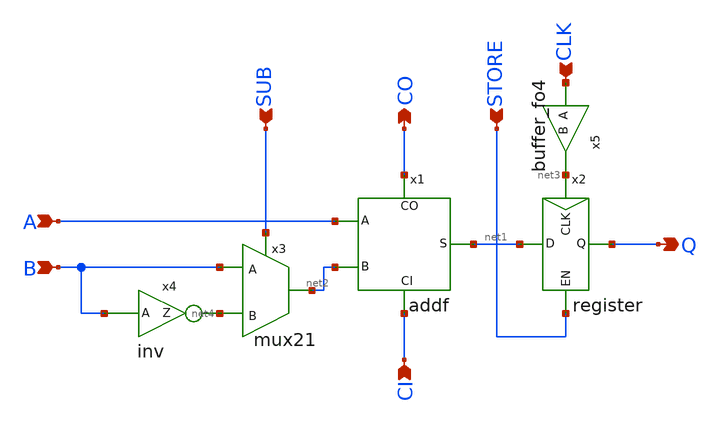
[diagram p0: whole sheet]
** sch_path: xschem/bitslice.sch
**.subckt bitslice A B CI CLK STORE CO Q SUB
*.ipin A
*.ipin B
*.ipin CI
*.ipin CLK
*.ipin STORE
*.opin CO
*.opin Q
*.ipin SUB
x1 A net2 CI net1 CO addf
x2 net3 STORE Q net1 register
x3 SUB B net2 net4 mux21
x4 net4 B inv
x5 net3 CLK buffer_fo4
**.ends

* expanding   symbol:  addf.sym # of pins=5
** sym_path: xschem/addf.sym
** sch_path: xschem/addf.sch
.subckt addf A B CI S CO
*.ipin A
*.ipin B
*.ipin CI
*.opin S
*.opin CO
XM1 theta CI mu GND sky130_fd_pr__nfet_01v8 L=0.15 W=0.42 nf=1 ad='int((nf+1)/2) * W/nf * 0.29' as='int((nf+2)/2) * W/nf * 0.29'
+ pd='2*int((nf+1)/2) * (W/nf + 0.29)' ps='2*int((nf+2)/2) * (W/nf + 0.29)' nrd='0.29 / W' nrs='0.29 / W'
+ sa=0 sb=0 sd=0 mult=1 m=1
XM2 theta CI lambda VDD sky130_fd_pr__pfet_01v8 L=0.15 W=0.42 nf=1 ad='int((nf+1)/2) * W/nf * 0.29' as='int((nf+2)/2) * W/nf * 0.29'
+ pd='2*int((nf+1)/2) * (W/nf + 0.29)' ps='2*int((nf+2)/2) * (W/nf + 0.29)' nrd='0.29 / W' nrs='0.29 / W'
+ sa=0 sb=0 sd=0 mult=1 m=1
XM3 lambda A VDD VDD sky130_fd_pr__pfet_01v8 L=0.15 W=0.42 nf=1 ad='int((nf+1)/2) * W/nf * 0.29' as='int((nf+2)/2) * W/nf * 0.29'
+ pd='2*int((nf+1)/2) * (W/nf + 0.29)' ps='2*int((nf+2)/2) * (W/nf + 0.29)' nrd='0.29 / W' nrs='0.29 / W'
+ sa=0 sb=0 sd=0 mult=1 m=1
XM4 lambda B VDD VDD sky130_fd_pr__pfet_01v8 L=0.15 W=0.42 nf=1 ad='int((nf+1)/2) * W/nf * 0.29' as='int((nf+2)/2) * W/nf * 0.29'
+ pd='2*int((nf+1)/2) * (W/nf + 0.29)' ps='2*int((nf+2)/2) * (W/nf + 0.29)' nrd='0.29 / W' nrs='0.29 / W'
+ sa=0 sb=0 sd=0 mult=1 m=1
XM5 mu A GND GND sky130_fd_pr__nfet_01v8 L=0.15 W=0.42 nf=1 ad='int((nf+1)/2) * W/nf * 0.29' as='int((nf+2)/2) * W/nf * 0.29'
+ pd='2*int((nf+1)/2) * (W/nf + 0.29)' ps='2*int((nf+2)/2) * (W/nf + 0.29)' nrd='0.29 / W' nrs='0.29 / W'
+ sa=0 sb=0 sd=0 mult=1 m=1
XM6 mu B GND GND sky130_fd_pr__nfet_01v8 L=0.15 W=0.42 nf=1 ad='int((nf+1)/2) * W/nf * 0.29' as='int((nf+2)/2) * W/nf * 0.29'
+ pd='2*int((nf+1)/2) * (W/nf + 0.29)' ps='2*int((nf+2)/2) * (W/nf + 0.29)' nrd='0.29 / W' nrs='0.29 / W'
+ sa=0 sb=0 sd=0 mult=1 m=1
XM7 theta B iota VDD sky130_fd_pr__pfet_01v8 L=0.15 W=0.42 nf=1 ad='int((nf+1)/2) * W/nf * 0.29' as='int((nf+2)/2) * W/nf * 0.29'
+ pd='2*int((nf+1)/2) * (W/nf + 0.29)' ps='2*int((nf+2)/2) * (W/nf + 0.29)' nrd='0.29 / W' nrs='0.29 / W'
+ sa=0 sb=0 sd=0 mult=1 m=1
XM8 iota A VDD VDD sky130_fd_pr__pfet_01v8 L=0.15 W=0.42 nf=1 ad='int((nf+1)/2) * W/nf * 0.29' as='int((nf+2)/2) * W/nf * 0.29'
+ pd='2*int((nf+1)/2) * (W/nf + 0.29)' ps='2*int((nf+2)/2) * (W/nf + 0.29)' nrd='0.29 / W' nrs='0.29 / W'
+ sa=0 sb=0 sd=0 mult=1 m=1
XM9 theta B kappa GND sky130_fd_pr__nfet_01v8 L=0.15 W=0.42 nf=1 ad='int((nf+1)/2) * W/nf * 0.29' as='int((nf+2)/2) * W/nf * 0.29'
+ pd='2*int((nf+1)/2) * (W/nf + 0.29)' ps='2*int((nf+2)/2) * (W/nf + 0.29)' nrd='0.29 / W' nrs='0.29 / W'
+ sa=0 sb=0 sd=0 mult=1 m=1
XM10 kappa A GND GND sky130_fd_pr__nfet_01v8 L=0.15 W=0.42 nf=1 ad='int((nf+1)/2) * W/nf * 0.29' as='int((nf+2)/2) * W/nf * 0.29'
+ pd='2*int((nf+1)/2) * (W/nf + 0.29)' ps='2*int((nf+2)/2) * (W/nf + 0.29)' nrd='0.29 / W' nrs='0.29 / W'
+ sa=0 sb=0 sd=0 mult=1 m=1
XM11 epsilon A VDD VDD sky130_fd_pr__pfet_01v8 L=0.15 W=0.42 nf=1 ad='int((nf+1)/2) * W/nf * 0.29' as='int((nf+2)/2) * W/nf * 0.29'
+ pd='2*int((nf+1)/2) * (W/nf + 0.29)' ps='2*int((nf+2)/2) * (W/nf + 0.29)' nrd='0.29 / W' nrs='0.29 / W'
+ sa=0 sb=0 sd=0 mult=1 m=1
XM12 epsilon B VDD VDD sky130_fd_pr__pfet_01v8 L=0.15 W=0.42 nf=1 ad='int((nf+1)/2) * W/nf * 0.29' as='int((nf+2)/2) * W/nf * 0.29'
+ pd='2*int((nf+1)/2) * (W/nf + 0.29)' ps='2*int((nf+2)/2) * (W/nf + 0.29)' nrd='0.29 / W' nrs='0.29 / W'
+ sa=0 sb=0 sd=0 mult=1 m=1
XM13 epsilon CI VDD VDD sky130_fd_pr__pfet_01v8 L=0.15 W=0.42 nf=1 ad='int((nf+1)/2) * W/nf * 0.29' as='int((nf+2)/2) * W/nf * 0.29'
+ pd='2*int((nf+1)/2) * (W/nf + 0.29)' ps='2*int((nf+2)/2) * (W/nf + 0.29)' nrd='0.29 / W' nrs='0.29 / W'
+ sa=0 sb=0 sd=0 mult=1 m=1
XM14 COM theta epsilon VDD sky130_fd_pr__pfet_01v8 L=0.15 W=0.42 nf=1 ad='int((nf+1)/2) * W/nf * 0.29'
+ as='int((nf+2)/2) * W/nf * 0.29' pd='2*int((nf+1)/2) * (W/nf + 0.29)' ps='2*int((nf+2)/2) * (W/nf + 0.29)'
+ nrd='0.29 / W' nrs='0.29 / W' sa=0 sb=0 sd=0 mult=1 m=1
XM15 COM theta zeta GND sky130_fd_pr__nfet_01v8 L=0.15 W=0.42 nf=1 ad='int((nf+1)/2) * W/nf * 0.29' as='int((nf+2)/2) * W/nf * 0.29'
+ pd='2*int((nf+1)/2) * (W/nf + 0.29)' ps='2*int((nf+2)/2) * (W/nf + 0.29)' nrd='0.29 / W' nrs='0.29 / W'
+ sa=0 sb=0 sd=0 mult=1 m=1
XM16 zeta A GND GND sky130_fd_pr__nfet_01v8 L=0.15 W=0.42 nf=1 ad='int((nf+1)/2) * W/nf * 0.29' as='int((nf+2)/2) * W/nf * 0.29'
+ pd='2*int((nf+1)/2) * (W/nf + 0.29)' ps='2*int((nf+2)/2) * (W/nf + 0.29)' nrd='0.29 / W' nrs='0.29 / W'
+ sa=0 sb=0 sd=0 mult=1 m=1
XM17 zeta B GND GND sky130_fd_pr__nfet_01v8 L=0.15 W=0.42 nf=1 ad='int((nf+1)/2) * W/nf * 0.29' as='int((nf+2)/2) * W/nf * 0.29'
+ pd='2*int((nf+1)/2) * (W/nf + 0.29)' ps='2*int((nf+2)/2) * (W/nf + 0.29)' nrd='0.29 / W' nrs='0.29 / W'
+ sa=0 sb=0 sd=0 mult=1 m=1
XM18 zeta CI GND GND sky130_fd_pr__nfet_01v8 L=0.15 W=0.42 nf=1 ad='int((nf+1)/2) * W/nf * 0.29' as='int((nf+2)/2) * W/nf * 0.29'
+ pd='2*int((nf+1)/2) * (W/nf + 0.29)' ps='2*int((nf+2)/2) * (W/nf + 0.29)' nrd='0.29 / W' nrs='0.29 / W'
+ sa=0 sb=0 sd=0 mult=1 m=1
XM19 COM B beta VDD sky130_fd_pr__pfet_01v8 L=0.15 W=0.42 nf=1 ad='int((nf+1)/2) * W/nf * 0.29' as='int((nf+2)/2) * W/nf * 0.29'
+ pd='2*int((nf+1)/2) * (W/nf + 0.29)' ps='2*int((nf+2)/2) * (W/nf + 0.29)' nrd='0.29 / W' nrs='0.29 / W'
+ sa=0 sb=0 sd=0 mult=1 m=1
XM20 beta CI alpha VDD sky130_fd_pr__pfet_01v8 L=0.15 W=0.42 nf=1 ad='int((nf+1)/2) * W/nf * 0.29' as='int((nf+2)/2) * W/nf * 0.29'
+ pd='2*int((nf+1)/2) * (W/nf + 0.29)' ps='2*int((nf+2)/2) * (W/nf + 0.29)' nrd='0.29 / W' nrs='0.29 / W'
+ sa=0 sb=0 sd=0 mult=1 m=1
XM21 alpha A VDD VDD sky130_fd_pr__pfet_01v8 L=0.15 W=0.42 nf=1 ad='int((nf+1)/2) * W/nf * 0.29' as='int((nf+2)/2) * W/nf * 0.29'
+ pd='2*int((nf+1)/2) * (W/nf + 0.29)' ps='2*int((nf+2)/2) * (W/nf + 0.29)' nrd='0.29 / W' nrs='0.29 / W'
+ sa=0 sb=0 sd=0 mult=1 m=1
XM22 COM B gamma GND sky130_fd_pr__nfet_01v8 L=0.15 W=0.42 nf=1 ad='int((nf+1)/2) * W/nf * 0.29' as='int((nf+2)/2) * W/nf * 0.29'
+ pd='2*int((nf+1)/2) * (W/nf + 0.29)' ps='2*int((nf+2)/2) * (W/nf + 0.29)' nrd='0.29 / W' nrs='0.29 / W'
+ sa=0 sb=0 sd=0 mult=1 m=1
XM23 gamma CI delta GND sky130_fd_pr__nfet_01v8 L=0.15 W=0.42 nf=1 ad='int((nf+1)/2) * W/nf * 0.29' as='int((nf+2)/2) * W/nf * 0.29'
+ pd='2*int((nf+1)/2) * (W/nf + 0.29)' ps='2*int((nf+2)/2) * (W/nf + 0.29)' nrd='0.29 / W' nrs='0.29 / W'
+ sa=0 sb=0 sd=0 mult=1 m=1
XM24 delta A GND GND sky130_fd_pr__nfet_01v8 L=0.15 W=0.42 nf=1 ad='int((nf+1)/2) * W/nf * 0.29' as='int((nf+2)/2) * W/nf * 0.29'
+ pd='2*int((nf+1)/2) * (W/nf + 0.29)' ps='2*int((nf+2)/2) * (W/nf + 0.29)' nrd='0.29 / W' nrs='0.29 / W'
+ sa=0 sb=0 sd=0 mult=1 m=1
XM25 CO theta GND GND sky130_fd_pr__nfet_01v8 L=0.15 W=0.42 nf=1 ad='int((nf+1)/2) * W/nf * 0.29' as='int((nf+2)/2) * W/nf * 0.29'
+ pd='2*int((nf+1)/2) * (W/nf + 0.29)' ps='2*int((nf+2)/2) * (W/nf + 0.29)' nrd='0.29 / W' nrs='0.29 / W'
+ sa=0 sb=0 sd=0 mult=1 m=1
XM26 CO theta VDD VDD sky130_fd_pr__pfet_01v8 L=0.15 W=0.42 nf=1 ad='int((nf+1)/2) * W/nf * 0.29' as='int((nf+2)/2) * W/nf * 0.29'
+ pd='2*int((nf+1)/2) * (W/nf + 0.29)' ps='2*int((nf+2)/2) * (W/nf + 0.29)' nrd='0.29 / W' nrs='0.29 / W'
+ sa=0 sb=0 sd=0 mult=1 m=1
XM27 S COM GND GND sky130_fd_pr__nfet_01v8 L=0.15 W=0.42 nf=1 ad='int((nf+1)/2) * W/nf * 0.29' as='int((nf+2)/2) * W/nf * 0.29'
+ pd='2*int((nf+1)/2) * (W/nf + 0.29)' ps='2*int((nf+2)/2) * (W/nf + 0.29)' nrd='0.29 / W' nrs='0.29 / W'
+ sa=0 sb=0 sd=0 mult=1 m=1
XM28 S COM VDD VDD sky130_fd_pr__pfet_01v8 L=0.15 W=0.42 nf=1 ad='int((nf+1)/2) * W/nf * 0.29' as='int((nf+2)/2) * W/nf * 0.29'
+ pd='2*int((nf+1)/2) * (W/nf + 0.29)' ps='2*int((nf+2)/2) * (W/nf + 0.29)' nrd='0.29 / W' nrs='0.29 / W'
+ sa=0 sb=0 sd=0 mult=1 m=1
.ends


* expanding   symbol:  register.sym # of pins=4
** sym_path: xschem/register.sym
** sch_path: xschem/register.sch
.subckt register CLK EN Q D
*.ipin CLK
*.ipin EN
*.ipin D
*.opin Q
x1 net1 Q D d_flip_flop
x2 CLK net1 EN and2
.ends


* expanding   symbol:  mux21.sym # of pins=4
** sym_path: xschem/mux21.sym
** sch_path: xschem/mux21.sch
.subckt mux21 S A Y B
*.ipin S
*.ipin A
*.ipin B
*.opin Y
x1 S A Y net1 t_gate
x2 net1 B Y S t_gate
x3 net1 S inv
.ends


* expanding   symbol:  inv.sym # of pins=2
** sym_path: xschem/inv.sym
** sch_path: xschem/inv.sch
.subckt inv Z A
*.ipin a
*.opin z
XM1 z a GND GND sky130_fd_pr__nfet_01v8 L=0.15 W=0.42 nf=1 ad='int((nf+1)/2) * W/nf * 0.29' as='int((nf+2)/2) * W/nf * 0.29'
+ pd='2*int((nf+1)/2) * (W/nf + 0.29)' ps='2*int((nf+2)/2) * (W/nf + 0.29)' nrd='0.29 / W' nrs='0.29 / W'
+ sa=0 sb=0 sd=0 mult=1 m=1
XM2 z a VDD VDD sky130_fd_pr__pfet_01v8 L=0.15 W=0.84 nf=1 ad='int((nf+1)/2) * W/nf * 0.29' as='int((nf+2)/2) * W/nf * 0.29'
+ pd='2*int((nf+1)/2) * (W/nf + 0.29)' ps='2*int((nf+2)/2) * (W/nf + 0.29)' nrd='0.29 / W' nrs='0.29 / W'
+ sa=0 sb=0 sd=0 mult=1 m=1
.ends


* expanding   symbol:  buffer_fo4.sym # of pins=2
** sym_path: xschem/buffer_fo4.sym
** sch_path: xschem/buffer_fo4.sch
.subckt buffer_fo4 B A
*.ipin A
*.opin B
XM1 net1 A GND GND sky130_fd_pr__nfet_01v8 L=0.15 W=0.42 nf=1 ad='int((nf+1)/2) * W/nf * 0.29' as='int((nf+2)/2) * W/nf * 0.29'
+ pd='2*int((nf+1)/2) * (W/nf + 0.29)' ps='2*int((nf+2)/2) * (W/nf + 0.29)' nrd='0.29 / W' nrs='0.29 / W'
+ sa=0 sb=0 sd=0 mult=1 m=1
XM2 B net1 GND GND sky130_fd_pr__nfet_01v8 L=0.15 W=1.68 nf=1 ad='int((nf+1)/2) * W/nf * 0.29' as='int((nf+2)/2) * W/nf * 0.29'
+ pd='2*int((nf+1)/2) * (W/nf + 0.29)' ps='2*int((nf+2)/2) * (W/nf + 0.29)' nrd='0.29 / W' nrs='0.29 / W'
+ sa=0 sb=0 sd=0 mult=1 m=1
XM3 net1 A VDD VDD sky130_fd_pr__pfet_01v8 L=0.15 W=0.84 nf=1 ad='int((nf+1)/2) * W/nf * 0.29' as='int((nf+2)/2) * W/nf * 0.29'
+ pd='2*int((nf+1)/2) * (W/nf + 0.29)' ps='2*int((nf+2)/2) * (W/nf + 0.29)' nrd='0.29 / W' nrs='0.29 / W'
+ sa=0 sb=0 sd=0 mult=1 m=1
XM4 B net1 VDD VDD sky130_fd_pr__pfet_01v8 L=0.15 W=3.36 nf=1 ad='int((nf+1)/2) * W/nf * 0.29' as='int((nf+2)/2) * W/nf * 0.29'
+ pd='2*int((nf+1)/2) * (W/nf + 0.29)' ps='2*int((nf+2)/2) * (W/nf + 0.29)' nrd='0.29 / W' nrs='0.29 / W'
+ sa=0 sb=0 sd=0 mult=1 m=1
.ends


* expanding   symbol:  d_flip_flop.sym # of pins=3
** sym_path: xschem/d_flip_flop.sym
** sch_path: xschem/d_flip_flop.sch
.subckt d_flip_flop clk Q D
*.ipin clk
*.ipin D
*.opin Q
XM1 clk_b clk GND GND sky130_fd_pr__nfet_01v8 L=0.15 W=0.84 nf=1 ad='int((nf+1)/2) * W/nf * 0.29' as='int((nf+2)/2) * W/nf * 0.29'
+ pd='2*int((nf+1)/2) * (W/nf + 0.29)' ps='2*int((nf+2)/2) * (W/nf + 0.29)' nrd='0.29 / W' nrs='0.29 / W'
+ sa=0 sb=0 sd=0 mult=1 m=1
XM2 clk_b clk VDD VDD sky130_fd_pr__pfet_01v8 L=0.15 W=1.68 nf=1 ad='int((nf+1)/2) * W/nf * 0.29' as='int((nf+2)/2) * W/nf * 0.29'
+ pd='2*int((nf+1)/2) * (W/nf + 0.29)' ps='2*int((nf+2)/2) * (W/nf + 0.29)' nrd='0.29 / W' nrs='0.29 / W'
+ sa=0 sb=0 sd=0 mult=1 m=1
XM3 net1 clk net6 VDD sky130_fd_pr__pfet_01v8 L=0.15 W=0.42 nf=1 ad='int((nf+1)/2) * W/nf * 0.29' as='int((nf+2)/2) * W/nf * 0.29'
+ pd='2*int((nf+1)/2) * (W/nf + 0.29)' ps='2*int((nf+2)/2) * (W/nf + 0.29)' nrd='0.29 / W' nrs='0.29 / W'
+ sa=0 sb=0 sd=0 mult=1 m=1
XM4 net6 D VDD VDD sky130_fd_pr__pfet_01v8 L=0.15 W=0.42 nf=1 ad='int((nf+1)/2) * W/nf * 0.29' as='int((nf+2)/2) * W/nf * 0.29'
+ pd='2*int((nf+1)/2) * (W/nf + 0.29)' ps='2*int((nf+2)/2) * (W/nf + 0.29)' nrd='0.29 / W' nrs='0.29 / W'
+ sa=0 sb=0 sd=0 mult=1 m=1
XM5 net1 clk_b net5 GND sky130_fd_pr__nfet_01v8 L=0.15 W=0.42 nf=1 ad='int((nf+1)/2) * W/nf * 0.29' as='int((nf+2)/2) * W/nf * 0.29'
+ pd='2*int((nf+1)/2) * (W/nf + 0.29)' ps='2*int((nf+2)/2) * (W/nf + 0.29)' nrd='0.29 / W' nrs='0.29 / W'
+ sa=0 sb=0 sd=0 mult=1 m=1
XM6 net5 D GND GND sky130_fd_pr__nfet_01v8 L=0.15 W=0.42 nf=1 ad='int((nf+1)/2) * W/nf * 0.29' as='int((nf+2)/2) * W/nf * 0.29'
+ pd='2*int((nf+1)/2) * (W/nf + 0.29)' ps='2*int((nf+2)/2) * (W/nf + 0.29)' nrd='0.29 / W' nrs='0.29 / W'
+ sa=0 sb=0 sd=0 mult=1 m=1
XM7 net2 net1 VDD VDD sky130_fd_pr__pfet_01v8 L=0.15 W=0.42 nf=1 ad='int((nf+1)/2) * W/nf * 0.29' as='int((nf+2)/2) * W/nf * 0.29'
+ pd='2*int((nf+1)/2) * (W/nf + 0.29)' ps='2*int((nf+2)/2) * (W/nf + 0.29)' nrd='0.29 / W' nrs='0.29 / W'
+ sa=0 sb=0 sd=0 mult=1 m=1
XM8 net2 net1 GND GND sky130_fd_pr__nfet_01v8 L=0.15 W=0.42 nf=1 ad='int((nf+1)/2) * W/nf * 0.29' as='int((nf+2)/2) * W/nf * 0.29'
+ pd='2*int((nf+1)/2) * (W/nf + 0.29)' ps='2*int((nf+2)/2) * (W/nf + 0.29)' nrd='0.29 / W' nrs='0.29 / W'
+ sa=0 sb=0 sd=0 mult=1 m=1
XM9 net1 clk_b net4 VDD sky130_fd_pr__pfet_01v8 L=0.15 W=0.42 nf=1 ad='int((nf+1)/2) * W/nf * 0.29' as='int((nf+2)/2) * W/nf * 0.29'
+ pd='2*int((nf+1)/2) * (W/nf + 0.29)' ps='2*int((nf+2)/2) * (W/nf + 0.29)' nrd='0.29 / W' nrs='0.29 / W'
+ sa=0 sb=0 sd=0 mult=1 m=1
XM10 net4 net2 VDD VDD sky130_fd_pr__pfet_01v8 L=0.15 W=0.42 nf=1 ad='int((nf+1)/2) * W/nf * 0.29' as='int((nf+2)/2) * W/nf * 0.29'
+ pd='2*int((nf+1)/2) * (W/nf + 0.29)' ps='2*int((nf+2)/2) * (W/nf + 0.29)' nrd='0.29 / W' nrs='0.29 / W'
+ sa=0 sb=0 sd=0 mult=1 m=1
XM11 net1 clk net3 GND sky130_fd_pr__nfet_01v8 L=0.15 W=0.42 nf=1 ad='int((nf+1)/2) * W/nf * 0.29' as='int((nf+2)/2) * W/nf * 0.29'
+ pd='2*int((nf+1)/2) * (W/nf + 0.29)' ps='2*int((nf+2)/2) * (W/nf + 0.29)' nrd='0.29 / W' nrs='0.29 / W'
+ sa=0 sb=0 sd=0 mult=1 m=1
XM12 net3 net2 GND GND sky130_fd_pr__nfet_01v8 L=0.15 W=0.42 nf=1 ad='int((nf+1)/2) * W/nf * 0.29' as='int((nf+2)/2) * W/nf * 0.29'
+ pd='2*int((nf+1)/2) * (W/nf + 0.29)' ps='2*int((nf+2)/2) * (W/nf + 0.29)' nrd='0.29 / W' nrs='0.29 / W'
+ sa=0 sb=0 sd=0 mult=1 m=1
XM13 net7 clk_b net9 VDD sky130_fd_pr__pfet_01v8 L=0.15 W=0.42 nf=1 ad='int((nf+1)/2) * W/nf * 0.29'
+ as='int((nf+2)/2) * W/nf * 0.29' pd='2*int((nf+1)/2) * (W/nf + 0.29)' ps='2*int((nf+2)/2) * (W/nf + 0.29)'
+ nrd='0.29 / W' nrs='0.29 / W' sa=0 sb=0 sd=0 mult=1 m=1
XM14 net9 net2 VDD VDD sky130_fd_pr__pfet_01v8 L=0.15 W=0.42 nf=1 ad='int((nf+1)/2) * W/nf * 0.29' as='int((nf+2)/2) * W/nf * 0.29'
+ pd='2*int((nf+1)/2) * (W/nf + 0.29)' ps='2*int((nf+2)/2) * (W/nf + 0.29)' nrd='0.29 / W' nrs='0.29 / W'
+ sa=0 sb=0 sd=0 mult=1 m=1
XM15 net7 clk net8 GND sky130_fd_pr__nfet_01v8 L=0.15 W=0.42 nf=1 ad='int((nf+1)/2) * W/nf * 0.29' as='int((nf+2)/2) * W/nf * 0.29'
+ pd='2*int((nf+1)/2) * (W/nf + 0.29)' ps='2*int((nf+2)/2) * (W/nf + 0.29)' nrd='0.29 / W' nrs='0.29 / W'
+ sa=0 sb=0 sd=0 mult=1 m=1
XM16 net8 net2 GND GND sky130_fd_pr__nfet_01v8 L=0.15 W=0.42 nf=1 ad='int((nf+1)/2) * W/nf * 0.29' as='int((nf+2)/2) * W/nf * 0.29'
+ pd='2*int((nf+1)/2) * (W/nf + 0.29)' ps='2*int((nf+2)/2) * (W/nf + 0.29)' nrd='0.29 / W' nrs='0.29 / W'
+ sa=0 sb=0 sd=0 mult=1 m=1
XM17 Q net7 VDD VDD sky130_fd_pr__pfet_01v8 L=0.15 W=0.84 nf=1 ad='int((nf+1)/2) * W/nf * 0.29' as='int((nf+2)/2) * W/nf * 0.29'
+ pd='2*int((nf+1)/2) * (W/nf + 0.29)' ps='2*int((nf+2)/2) * (W/nf + 0.29)' nrd='0.29 / W' nrs='0.29 / W'
+ sa=0 sb=0 sd=0 mult=1 m=1
XM18 Q net7 GND GND sky130_fd_pr__nfet_01v8 L=0.15 W=0.42 nf=1 ad='int((nf+1)/2) * W/nf * 0.29' as='int((nf+2)/2) * W/nf * 0.29'
+ pd='2*int((nf+1)/2) * (W/nf + 0.29)' ps='2*int((nf+2)/2) * (W/nf + 0.29)' nrd='0.29 / W' nrs='0.29 / W'
+ sa=0 sb=0 sd=0 mult=1 m=1
XM19 net7 clk net11 VDD sky130_fd_pr__pfet_01v8 L=0.15 W=0.42 nf=1 ad='int((nf+1)/2) * W/nf * 0.29' as='int((nf+2)/2) * W/nf * 0.29'
+ pd='2*int((nf+1)/2) * (W/nf + 0.29)' ps='2*int((nf+2)/2) * (W/nf + 0.29)' nrd='0.29 / W' nrs='0.29 / W'
+ sa=0 sb=0 sd=0 mult=1 m=1
XM20 net11 Q VDD VDD sky130_fd_pr__pfet_01v8 L=0.15 W=0.42 nf=1 ad='int((nf+1)/2) * W/nf * 0.29' as='int((nf+2)/2) * W/nf * 0.29'
+ pd='2*int((nf+1)/2) * (W/nf + 0.29)' ps='2*int((nf+2)/2) * (W/nf + 0.29)' nrd='0.29 / W' nrs='0.29 / W'
+ sa=0 sb=0 sd=0 mult=1 m=1
XM21 net7 clk_b net10 GND sky130_fd_pr__nfet_01v8 L=0.15 W=0.42 nf=1 ad='int((nf+1)/2) * W/nf * 0.29'
+ as='int((nf+2)/2) * W/nf * 0.29' pd='2*int((nf+1)/2) * (W/nf + 0.29)' ps='2*int((nf+2)/2) * (W/nf + 0.29)'
+ nrd='0.29 / W' nrs='0.29 / W' sa=0 sb=0 sd=0 mult=1 m=1
XM22 net10 Q GND GND sky130_fd_pr__nfet_01v8 L=0.15 W=0.42 nf=1 ad='int((nf+1)/2) * W/nf * 0.29' as='int((nf+2)/2) * W/nf * 0.29'
+ pd='2*int((nf+1)/2) * (W/nf + 0.29)' ps='2*int((nf+2)/2) * (W/nf + 0.29)' nrd='0.29 / W' nrs='0.29 / W'
+ sa=0 sb=0 sd=0 mult=1 m=1
.ends


* expanding   symbol:  and2.sym # of pins=3
** sym_path: xschem/and2.sym
** sch_path: xschem/and2.sch
.subckt and2 A Y B
*.ipin A
*.ipin B
*.opin Y
XM1 net1 A net2 GND sky130_fd_pr__nfet_01v8 L=0.15 W=0.84 nf=1 ad='int((nf+1)/2) * W/nf * 0.29' as='int((nf+2)/2) * W/nf * 0.29'
+ pd='2*int((nf+1)/2) * (W/nf + 0.29)' ps='2*int((nf+2)/2) * (W/nf + 0.29)' nrd='0.29 / W' nrs='0.29 / W'
+ sa=0 sb=0 sd=0 mult=1 m=1
XM2 net2 B gnd GND sky130_fd_pr__nfet_01v8 L=0.15 W=0.84 nf=1 ad='int((nf+1)/2) * W/nf * 0.29' as='int((nf+2)/2) * W/nf * 0.29'
+ pd='2*int((nf+1)/2) * (W/nf + 0.29)' ps='2*int((nf+2)/2) * (W/nf + 0.29)' nrd='0.29 / W' nrs='0.29 / W'
+ sa=0 sb=0 sd=0 mult=1 m=1
XM3 net1 B vdd VDD sky130_fd_pr__pfet_01v8 L=0.15 W=0.84 nf=1 ad='int((nf+1)/2) * W/nf * 0.29' as='int((nf+2)/2) * W/nf * 0.29'
+ pd='2*int((nf+1)/2) * (W/nf + 0.29)' ps='2*int((nf+2)/2) * (W/nf + 0.29)' nrd='0.29 / W' nrs='0.29 / W'
+ sa=0 sb=0 sd=0 mult=1 m=1
XM4 net1 A vdd VDD sky130_fd_pr__pfet_01v8 L=0.15 W=0.84 nf=1 ad='int((nf+1)/2) * W/nf * 0.29' as='int((nf+2)/2) * W/nf * 0.29'
+ pd='2*int((nf+1)/2) * (W/nf + 0.29)' ps='2*int((nf+2)/2) * (W/nf + 0.29)' nrd='0.29 / W' nrs='0.29 / W'
+ sa=0 sb=0 sd=0 mult=1 m=1
XM5 Y net1 vdd VDD sky130_fd_pr__pfet_01v8 L=0.15 W=0.84 nf=1 ad='int((nf+1)/2) * W/nf * 0.29' as='int((nf+2)/2) * W/nf * 0.29'
+ pd='2*int((nf+1)/2) * (W/nf + 0.29)' ps='2*int((nf+2)/2) * (W/nf + 0.29)' nrd='0.29 / W' nrs='0.29 / W'
+ sa=0 sb=0 sd=0 mult=1 m=1
XM6 Y net1 gnd GND sky130_fd_pr__nfet_01v8 L=0.15 W=0.42 nf=1 ad='int((nf+1)/2) * W/nf * 0.29' as='int((nf+2)/2) * W/nf * 0.29'
+ pd='2*int((nf+1)/2) * (W/nf + 0.29)' ps='2*int((nf+2)/2) * (W/nf + 0.29)' nrd='0.29 / W' nrs='0.29 / W'
+ sa=0 sb=0 sd=0 mult=1 m=1
.ends


* expanding   symbol:  t_gate.sym # of pins=4
** sym_path: xschem/t_gate.sym
** sch_path: xschem/t_gate.sch
.subckt t_gate E_n in out E
*.ipin in
*.opin out
*.ipin E
*.ipin E_n
XM1 in E out GND sky130_fd_pr__nfet_01v8 L=0.15 W=0.42 nf=1 ad='int((nf+1)/2) * W/nf * 0.29' as='int((nf+2)/2) * W/nf * 0.29'
+ pd='2*int((nf+1)/2) * (W/nf + 0.29)' ps='2*int((nf+2)/2) * (W/nf + 0.29)' nrd='0.29 / W' nrs='0.29 / W'
+ sa=0 sb=0 sd=0 mult=1 m=1
XM2 in E_n out VDD sky130_fd_pr__pfet_01v8 L=0.15 W=0.84 nf=1 ad='int((nf+1)/2) * W/nf * 0.29' as='int((nf+2)/2) * W/nf * 0.29'
+ pd='2*int((nf+1)/2) * (W/nf + 0.29)' ps='2*int((nf+2)/2) * (W/nf + 0.29)' nrd='0.29 / W' nrs='0.29 / W'
+ sa=0 sb=0 sd=0 mult=1 m=1
.ends

.GLOBAL VDD
.GLOBAL GND
.GLOBAL gnd
.GLOBAL vdd
.end
